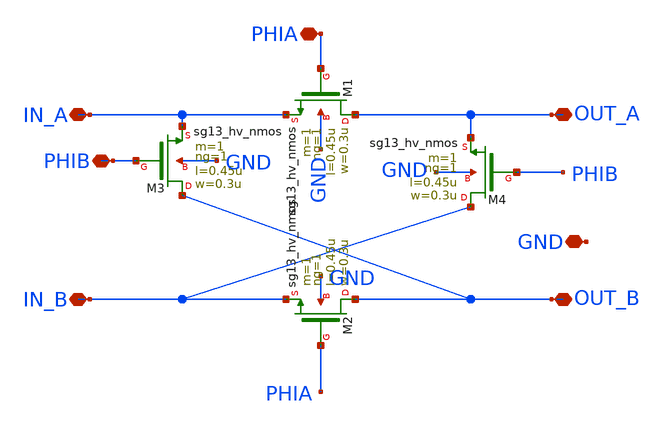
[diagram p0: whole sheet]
** sch_path: dependencies/OTA/OTA-main/schematic/xschem/CHOPPER.sch
**.subckt CHOPPER IN_A IN_B OUT_B OUT_A PHIA PHIB GND
*.iopin IN_A
*.iopin IN_B
*.iopin OUT_B
*.iopin OUT_A
*.iopin PHIA
*.iopin PHIB
*.iopin GND
XM1 OUT_A PHIA IN_A GND sg13_hv_nmos w=0.3u l=0.45u ng=1 m=1 mm_ok=1
XM2 OUT_B PHIA IN_B GND sg13_hv_nmos w=0.3u l=0.45u ng=1 m=1 mm_ok=1
XM3 OUT_B PHIB IN_A GND sg13_hv_nmos w=0.3u l=0.45u ng=1 m=1 mm_ok=1
XM4 IN_B PHIB OUT_A GND sg13_hv_nmos w=0.3u l=0.45u ng=1 m=1 mm_ok=1
**.ends
.end
